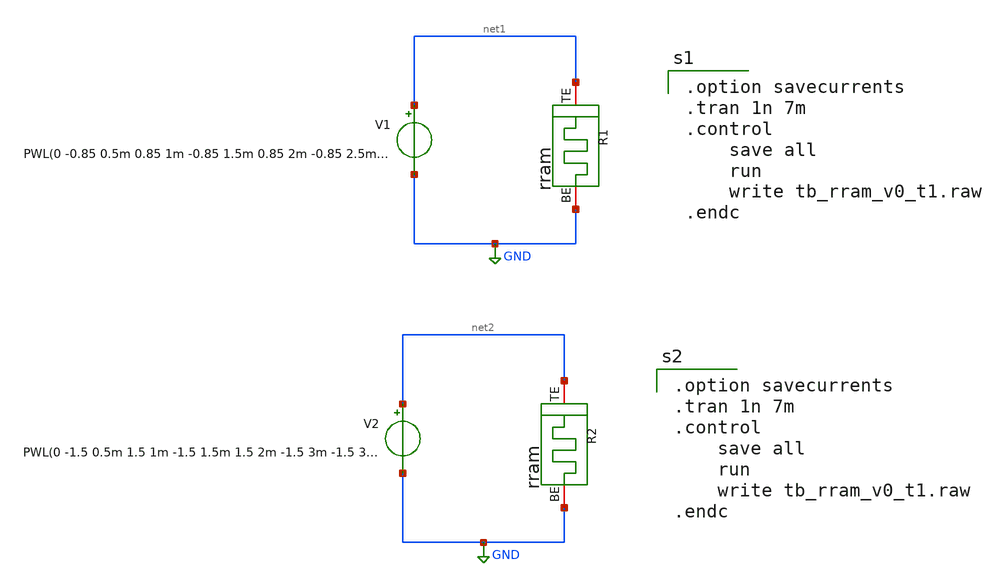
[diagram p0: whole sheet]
** sch_path: designs/tb_memristor/tb_rram_v0_t1.sch
**.subckt tb_rram_v0_t1
V1 net1 GND PWL(0 -0.85 0.5m 0.85 1m -0.85 1.5m 0.85 2m -0.85 2.5m 0.85 3m -0.85 3.5m 0.85 4m -0.85
+ 4.5m 0.85 5m -0.85 5.5m 0.85 6m -0.85 6.5m 0.85 7m -0.85)
.save i(v1)
R1 net1 GND rram
V2 net2 GND PWL(0 -1.5 0.5m 1.5 1m -1.5 1.5m 1.5 2m -1.5 3m -1.5 3.5m 1.5)
.save i(v2)
R2 net2 GND rram
**** begin user architecture code

.option savecurrents
.tran 1n 7m
.control
	save all
	run
	write tb_rram_v0_t1.raw
.endc


.subckt rram BE TE
N1 BE TE rram_model
.model rram_model rram_va
.ends rram

.control
pre_osdi /foss/designs/spike_130/designs/memristors/rram_v0/rram.osdi
.endc


.option savecurrents
.tran 1n 7m
.control
	save all
	run
	write tb_rram_v0_t1.raw
.endc

**** end user architecture code
**.ends
.GLOBAL GND
.end
